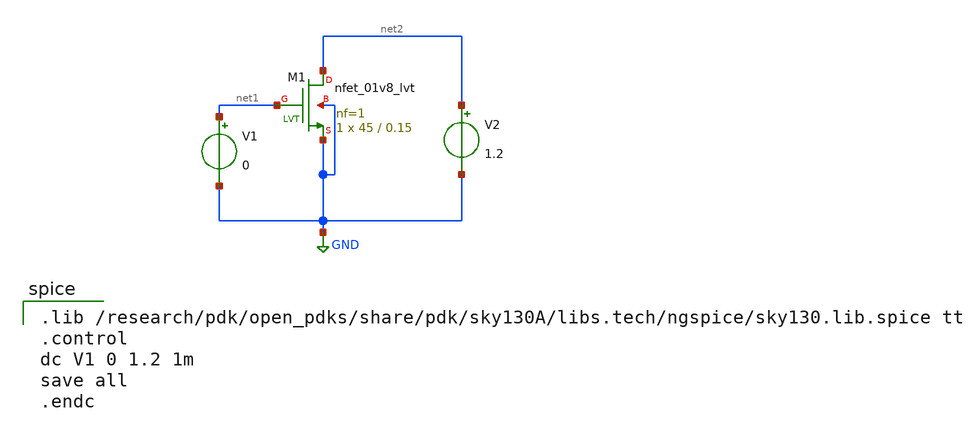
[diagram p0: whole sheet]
** sch_path: skywater_stuff/ECE631_RF_CMOS/device_sweep.sch
**.subckt device_sweep
XM1 net2 net1 GND GND sky130_fd_pr__nfet_01v8_lvt L=0.15 W=45 nf=1 ad='int((nf+1)/2) * W/nf * 0.29' as='int((nf+2)/2) * W/nf * 0.29'
+ pd='2*int((nf+1)/2) * (W/nf + 0.29)' ps='2*int((nf+2)/2) * (W/nf + 0.29)' nrd='0.29 / W' nrs='0.29 / W'
+ sa=0 sb=0 sd=0 mult=1 m=1
V1 net1 GND 0
V2 net2 GND 1.2
**** begin user architecture code

.lib /research/pdk/open_pdks/share/pdk/sky130A/libs.tech/ngspice/sky130.lib.spice tt
.control
dc V1 0 1.2 1m
save all
.endc


**** end user architecture code
**.ends
.GLOBAL GND
.end
